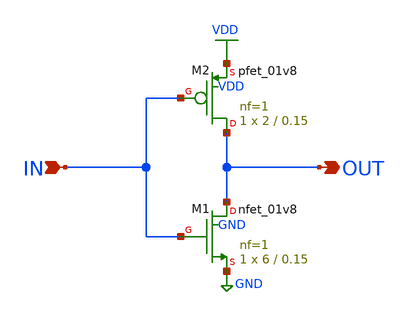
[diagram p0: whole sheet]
** sch_path: saafirah_tugas1_dsrt2026.sch
**.subckt saafirah_tugas1_dsrt2026 IN OUT
*.ipin IN
*.opin OUT
XM1 OUT IN GND GND sky130_fd_pr__nfet_01v8 L=0.15 W=6 nf=1 ad='int((1 + 1)/2) * 6 / 1 * 0.29' as='int((1 + 2)/2) * 6 / 1 * 0.29'
+ pd='2*int((1 + 1)/2) * (6 / 1 + 0.29)' ps='2*int((1 + 2)/2) * (6 / 1 + 0.29)' nrd='0.29 / 6 ' nrs='0.29 / 6 '
+ sa=0 sb=0 sd=0 mult=1 m=1
XM2 OUT IN VDD VDD sky130_fd_pr__pfet_01v8 L=0.15 W=2 nf=1 ad='int((1 + 1)/2) * 2 / 1 * 0.29' as='int((1 + 2)/2) * 2 / 1 * 0.29'
+ pd='2*int((1 + 1)/2) * (2 / 1 + 0.29)' ps='2*int((1 + 2)/2) * (2 / 1 + 0.29)' nrd='0.29 / 2 ' nrs='0.29 / 2 '
+ sa=0 sb=0 sd=0 mult=1 m=1
**.ends
.GLOBAL VDD
.GLOBAL GND
.end
